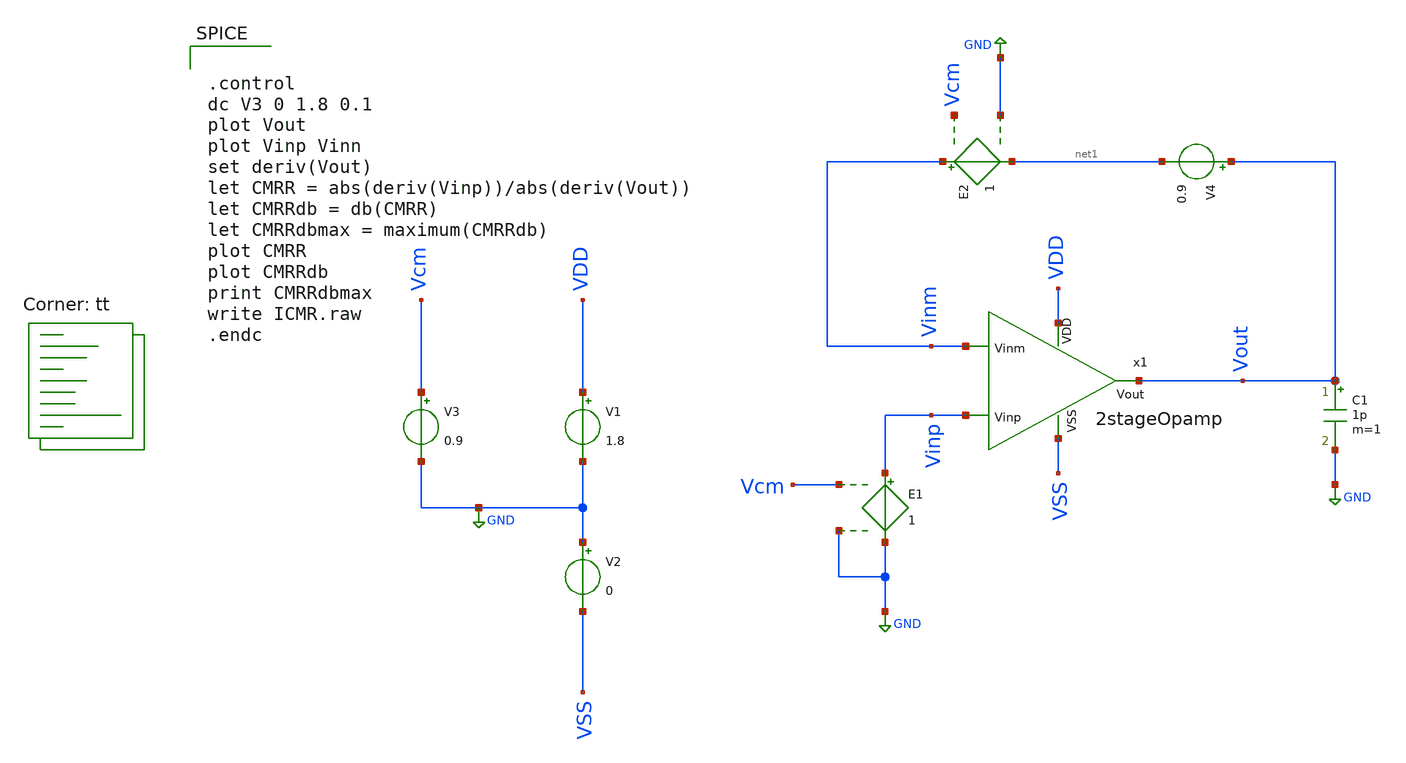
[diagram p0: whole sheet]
** sch_path: xschem/TestBenches/ICMR.sch
**.subckt ICMR
V1 VDD GND 1.8
V2 GND VSS 0
V3 Vcm GND 0.9
x1 VDD Vinm Vinp Vout VSS 2stageOpamp
E1 Vinp GND Vcm GND 1
E2 Vinm net1 Vcm GND 1
V4 Vout net1 0.9
C1 Vout GND 1p m=1
**** begin user architecture code


.control
dc V3 0 1.8 0.1
plot Vout
plot Vinp Vinn
set deriv(Vout)
let CMRR = abs(deriv(Vinp))/abs(deriv(Vout))
let CMRRdb = db(CMRR)
let CMRRdbmax = maximum(CMRRdb)
plot CMRR
plot CMRRdb
print CMRRdbmax
write ICMR.raw
.endc



.lib $::SKYWATER_MODELS/sky130.lib.spice tt
**** end user architecture code
**.ends
.GLOBAL GND
.end
